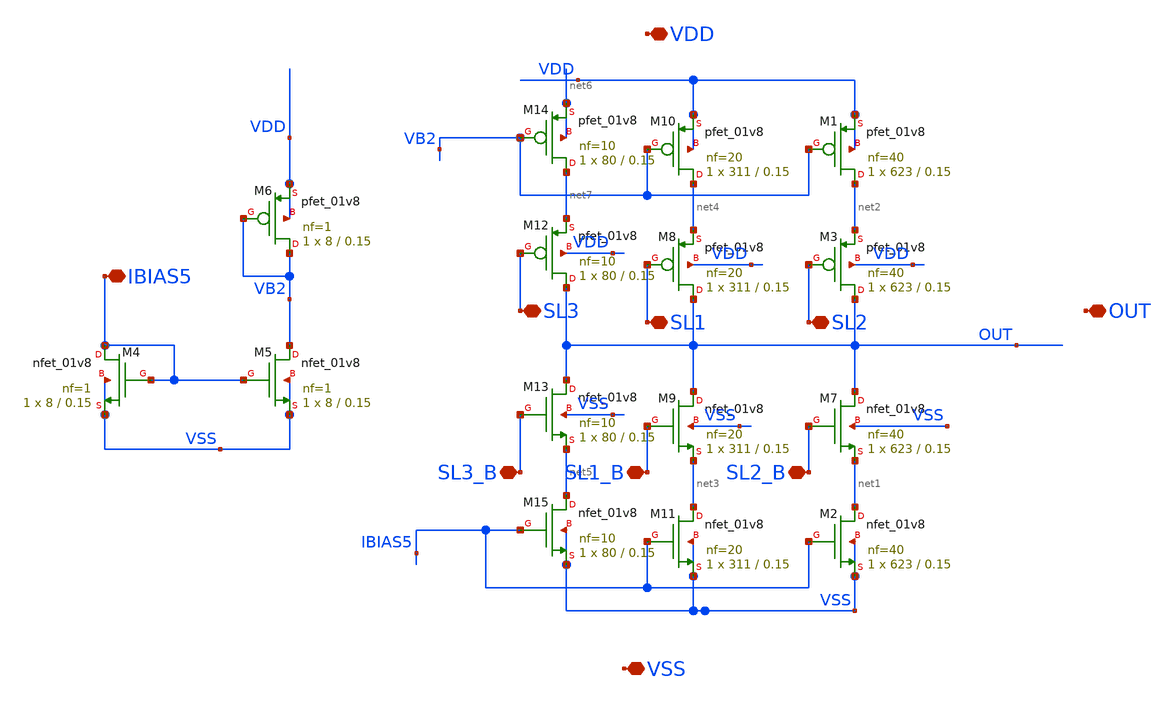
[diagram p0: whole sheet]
** sch_path: xschem/DC_DC_Converter_xschem/DC_DC_Converter/Current_pump_mirror/current_pump_mirror_three_brunch_symbol.sch
**.subckt current_pump_mirror_three_brunch_symbol SL3 SL1 VDD VSS OUT SL2 IBIAS5 SL3_B SL1_B SL2_B
*.iopin SL3
*.iopin SL1
*.iopin VDD
*.iopin VSS
*.iopin OUT
*.iopin SL2
*.iopin IBIAS5
*.iopin SL3_B
*.iopin SL1_B
*.iopin SL2_B
XM3 OUT SL2 net2 VDD sky130_fd_pr__pfet_01v8 L=0.15 W=623 nf=40 ad='int((nf+1)/2) * W/nf * 0.29' as='int((nf+2)/2) * W/nf * 0.29'
+ pd='2*int((nf+1)/2) * (W/nf + 0.29)' ps='2*int((nf+2)/2) * (W/nf + 0.29)' nrd='0.29 / W' nrs='0.29 / W'
+ sa=0 sb=0 sd=0 mult=1 m=1
XM7 OUT SL2_B net1 VSS sky130_fd_pr__nfet_01v8 L=0.15 W=623 nf=40 ad='int((nf+1)/2) * W/nf * 0.29' as='int((nf+2)/2) * W/nf * 0.29'
+ pd='2*int((nf+1)/2) * (W/nf + 0.29)' ps='2*int((nf+2)/2) * (W/nf + 0.29)' nrd='0.29 / W' nrs='0.29 / W'
+ sa=0 sb=0 sd=0 mult=1 m=1
XM1 net2 VB2 VDD VDD sky130_fd_pr__pfet_01v8 L=0.15 W=623 nf=40 ad='int((nf+1)/2) * W/nf * 0.29' as='int((nf+2)/2) * W/nf * 0.29'
+ pd='2*int((nf+1)/2) * (W/nf + 0.29)' ps='2*int((nf+2)/2) * (W/nf + 0.29)' nrd='0.29 / W' nrs='0.29 / W'
+ sa=0 sb=0 sd=0 mult=1 m=1
XM2 net1 IBIAS5 VSS VSS sky130_fd_pr__nfet_01v8 L=0.15 W=623 nf=40 ad='int((nf+1)/2) * W/nf * 0.29' as='int((nf+2)/2) * W/nf * 0.29'
+ pd='2*int((nf+1)/2) * (W/nf + 0.29)' ps='2*int((nf+2)/2) * (W/nf + 0.29)' nrd='0.29 / W' nrs='0.29 / W'
+ sa=0 sb=0 sd=0 mult=1 m=1
XM4 IBIAS5 IBIAS5 VSS VSS sky130_fd_pr__nfet_01v8 L=0.15 W=8 nf=1 ad='int((nf+1)/2) * W/nf * 0.29' as='int((nf+2)/2) * W/nf * 0.29'
+ pd='2*int((nf+1)/2) * (W/nf + 0.29)' ps='2*int((nf+2)/2) * (W/nf + 0.29)' nrd='0.29 / W' nrs='0.29 / W'
+ sa=0 sb=0 sd=0 mult=1 m=1
XM5 VB2 IBIAS5 VSS VSS sky130_fd_pr__nfet_01v8 L=0.15 W=8 nf=1 ad='int((nf+1)/2) * W/nf * 0.29' as='int((nf+2)/2) * W/nf * 0.29'
+ pd='2*int((nf+1)/2) * (W/nf + 0.29)' ps='2*int((nf+2)/2) * (W/nf + 0.29)' nrd='0.29 / W' nrs='0.29 / W'
+ sa=0 sb=0 sd=0 mult=1 m=1
XM6 VB2 VB2 VDD VDD sky130_fd_pr__pfet_01v8 L=0.15 W=8 nf=1 ad='int((nf+1)/2) * W/nf * 0.29' as='int((nf+2)/2) * W/nf * 0.29'
+ pd='2*int((nf+1)/2) * (W/nf + 0.29)' ps='2*int((nf+2)/2) * (W/nf + 0.29)' nrd='0.29 / W' nrs='0.29 / W'
+ sa=0 sb=0 sd=0 mult=1 m=1
XM8 OUT SL1 net4 VDD sky130_fd_pr__pfet_01v8 L=0.15 W=311 nf=20 ad='int((nf+1)/2) * W/nf * 0.29' as='int((nf+2)/2) * W/nf * 0.29'
+ pd='2*int((nf+1)/2) * (W/nf + 0.29)' ps='2*int((nf+2)/2) * (W/nf + 0.29)' nrd='0.29 / W' nrs='0.29 / W'
+ sa=0 sb=0 sd=0 mult=1 m=1
XM9 OUT SL1_B net3 VSS sky130_fd_pr__nfet_01v8 L=0.15 W=311 nf=20 ad='int((nf+1)/2) * W/nf * 0.29' as='int((nf+2)/2) * W/nf * 0.29'
+ pd='2*int((nf+1)/2) * (W/nf + 0.29)' ps='2*int((nf+2)/2) * (W/nf + 0.29)' nrd='0.29 / W' nrs='0.29 / W'
+ sa=0 sb=0 sd=0 mult=1 m=1
XM10 net4 VB2 VDD VDD sky130_fd_pr__pfet_01v8 L=0.15 W=311 nf=20 ad='int((nf+1)/2) * W/nf * 0.29' as='int((nf+2)/2) * W/nf * 0.29'
+ pd='2*int((nf+1)/2) * (W/nf + 0.29)' ps='2*int((nf+2)/2) * (W/nf + 0.29)' nrd='0.29 / W' nrs='0.29 / W'
+ sa=0 sb=0 sd=0 mult=1 m=1
XM11 net3 IBIAS5 VSS VSS sky130_fd_pr__nfet_01v8 L=0.15 W=311 nf=20 ad='int((nf+1)/2) * W/nf * 0.29'
+ as='int((nf+2)/2) * W/nf * 0.29' pd='2*int((nf+1)/2) * (W/nf + 0.29)' ps='2*int((nf+2)/2) * (W/nf + 0.29)'
+ nrd='0.29 / W' nrs='0.29 / W' sa=0 sb=0 sd=0 mult=1 m=1
XM12 OUT SL3 net7 VDD sky130_fd_pr__pfet_01v8 L=0.15 W=80 nf=10 ad='int((nf+1)/2) * W/nf * 0.29' as='int((nf+2)/2) * W/nf * 0.29'
+ pd='2*int((nf+1)/2) * (W/nf + 0.29)' ps='2*int((nf+2)/2) * (W/nf + 0.29)' nrd='0.29 / W' nrs='0.29 / W'
+ sa=0 sb=0 sd=0 mult=1 m=1
XM13 OUT SL3_B net5 VSS sky130_fd_pr__nfet_01v8 L=0.15 W=80 nf=10 ad='int((nf+1)/2) * W/nf * 0.29' as='int((nf+2)/2) * W/nf * 0.29'
+ pd='2*int((nf+1)/2) * (W/nf + 0.29)' ps='2*int((nf+2)/2) * (W/nf + 0.29)' nrd='0.29 / W' nrs='0.29 / W'
+ sa=0 sb=0 sd=0 mult=1 m=1
XM14 net7 VB2 net6 net6 sky130_fd_pr__pfet_01v8 L=0.15 W=80 nf=10 ad='int((nf+1)/2) * W/nf * 0.29' as='int((nf+2)/2) * W/nf * 0.29'
+ pd='2*int((nf+1)/2) * (W/nf + 0.29)' ps='2*int((nf+2)/2) * (W/nf + 0.29)' nrd='0.29 / W' nrs='0.29 / W'
+ sa=0 sb=0 sd=0 mult=1 m=1
XM15 net5 IBIAS5 VSS VSS sky130_fd_pr__nfet_01v8 L=0.15 W=80 nf=10 ad='int((nf+1)/2) * W/nf * 0.29' as='int((nf+2)/2) * W/nf * 0.29'
+ pd='2*int((nf+1)/2) * (W/nf + 0.29)' ps='2*int((nf+2)/2) * (W/nf + 0.29)' nrd='0.29 / W' nrs='0.29 / W'
+ sa=0 sb=0 sd=0 mult=1 m=1
**.ends
.end
